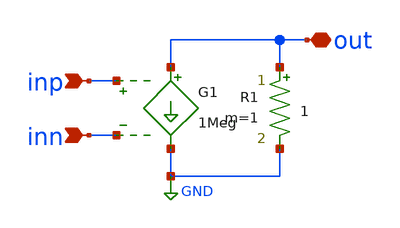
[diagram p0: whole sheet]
** sch_path: prj/template/2_Idealized_circuits/ideal_opamp.sch
**.subckt ideal_opamp out inp inn
*.iopin out
*.ipin inp
*.ipin inn
G1 out GND inp inn 1Meg
R1 out GND 1 m=1
**.ends
.GLOBAL GND
.end
